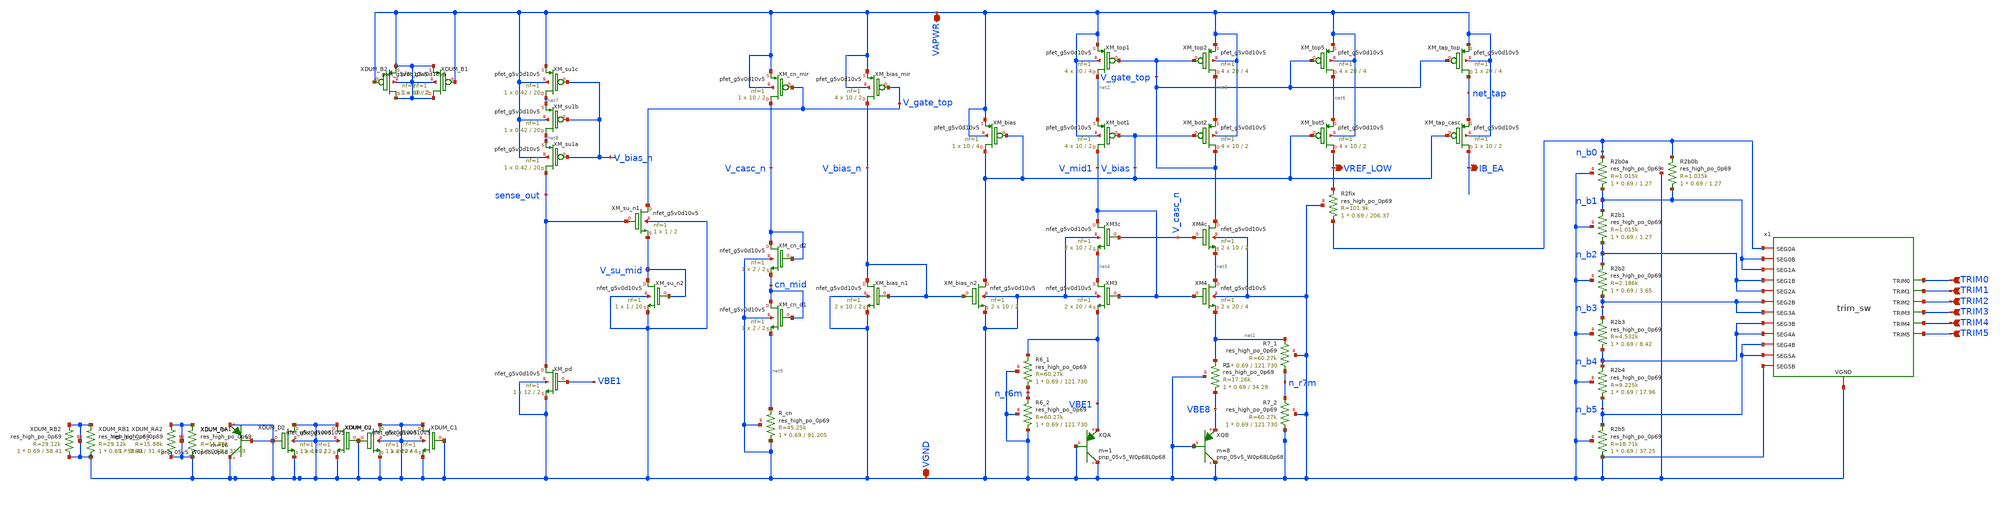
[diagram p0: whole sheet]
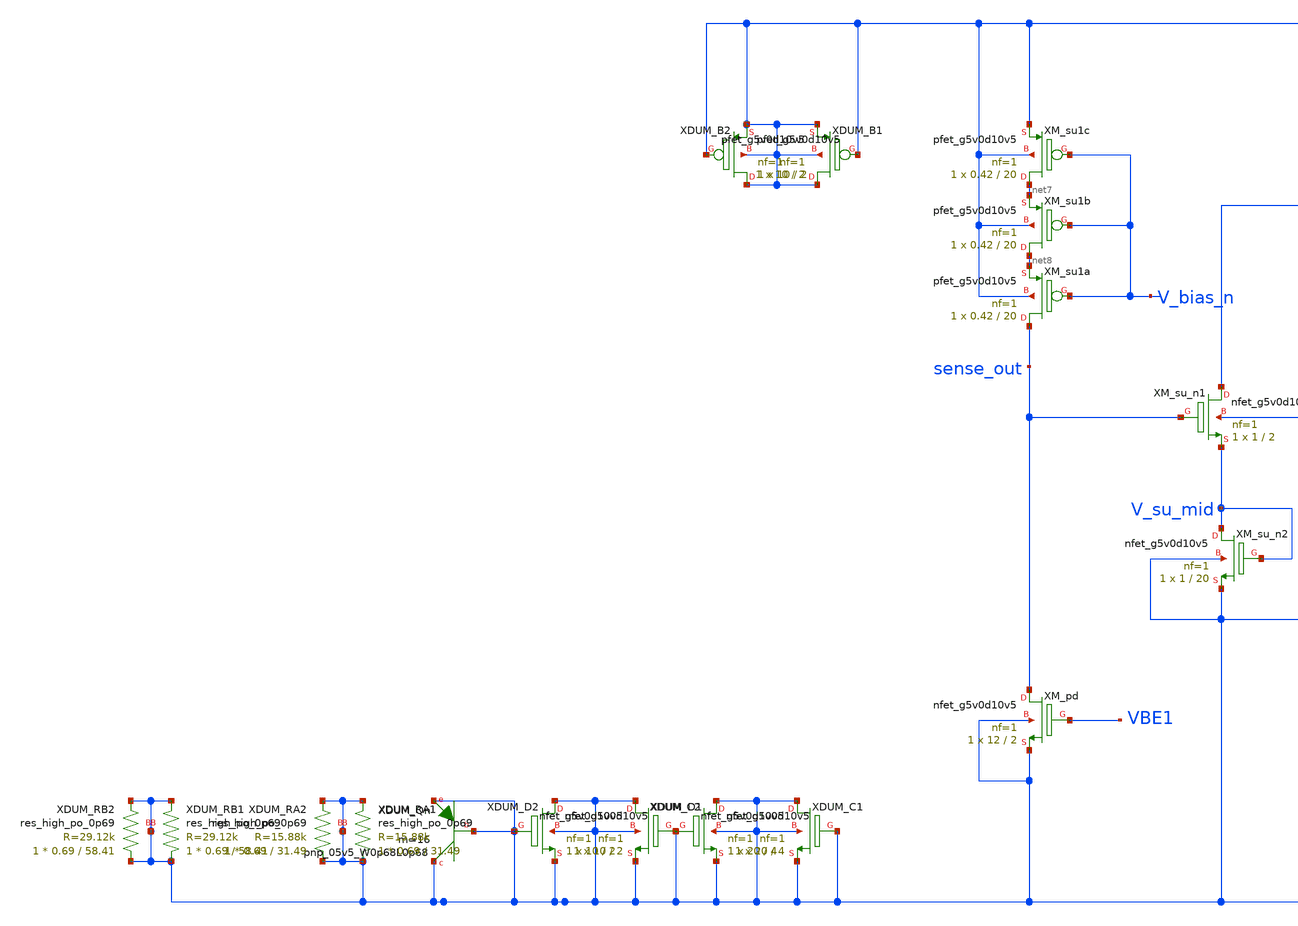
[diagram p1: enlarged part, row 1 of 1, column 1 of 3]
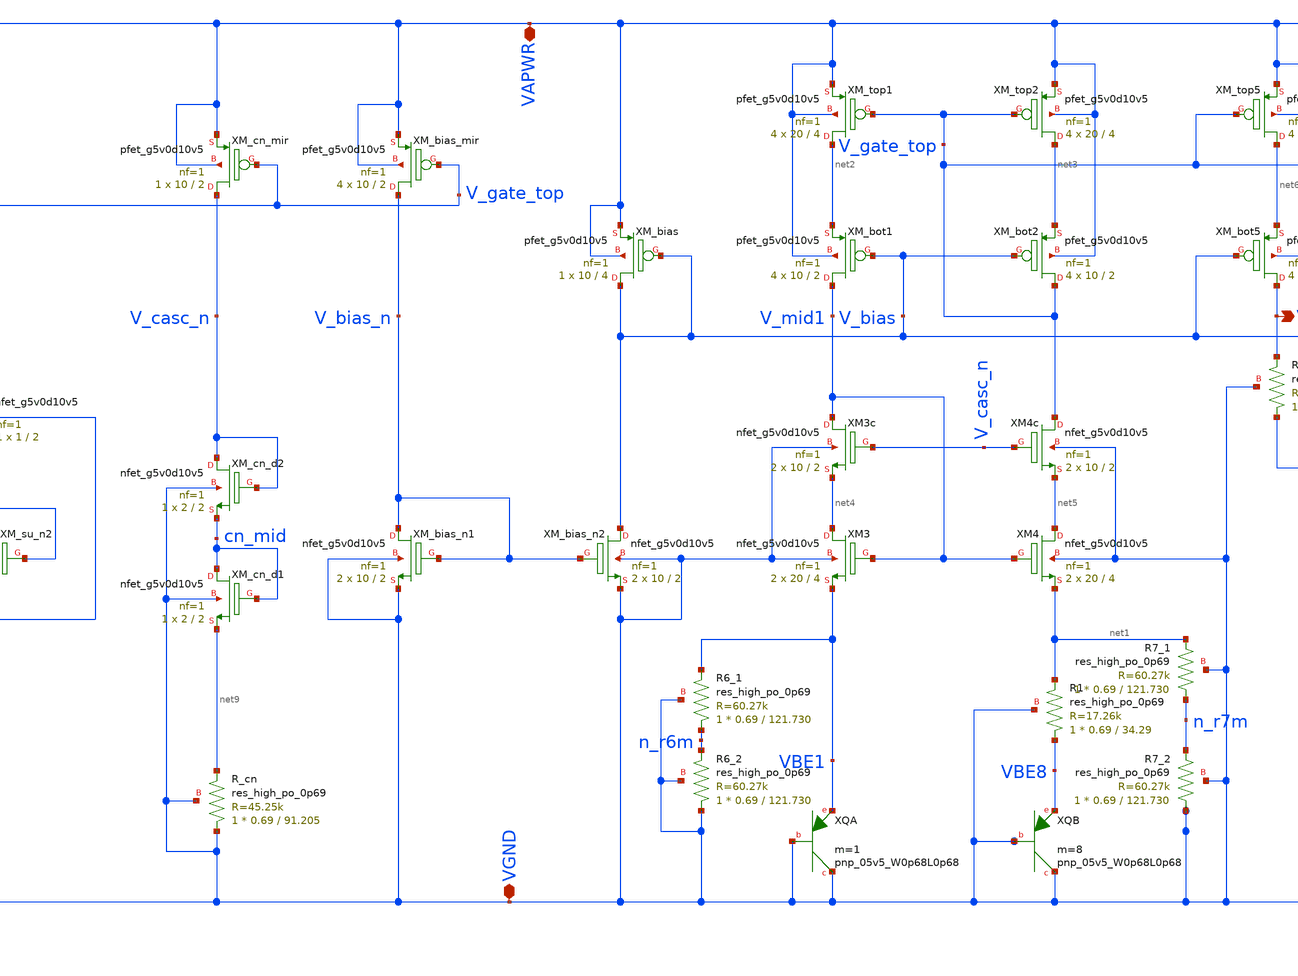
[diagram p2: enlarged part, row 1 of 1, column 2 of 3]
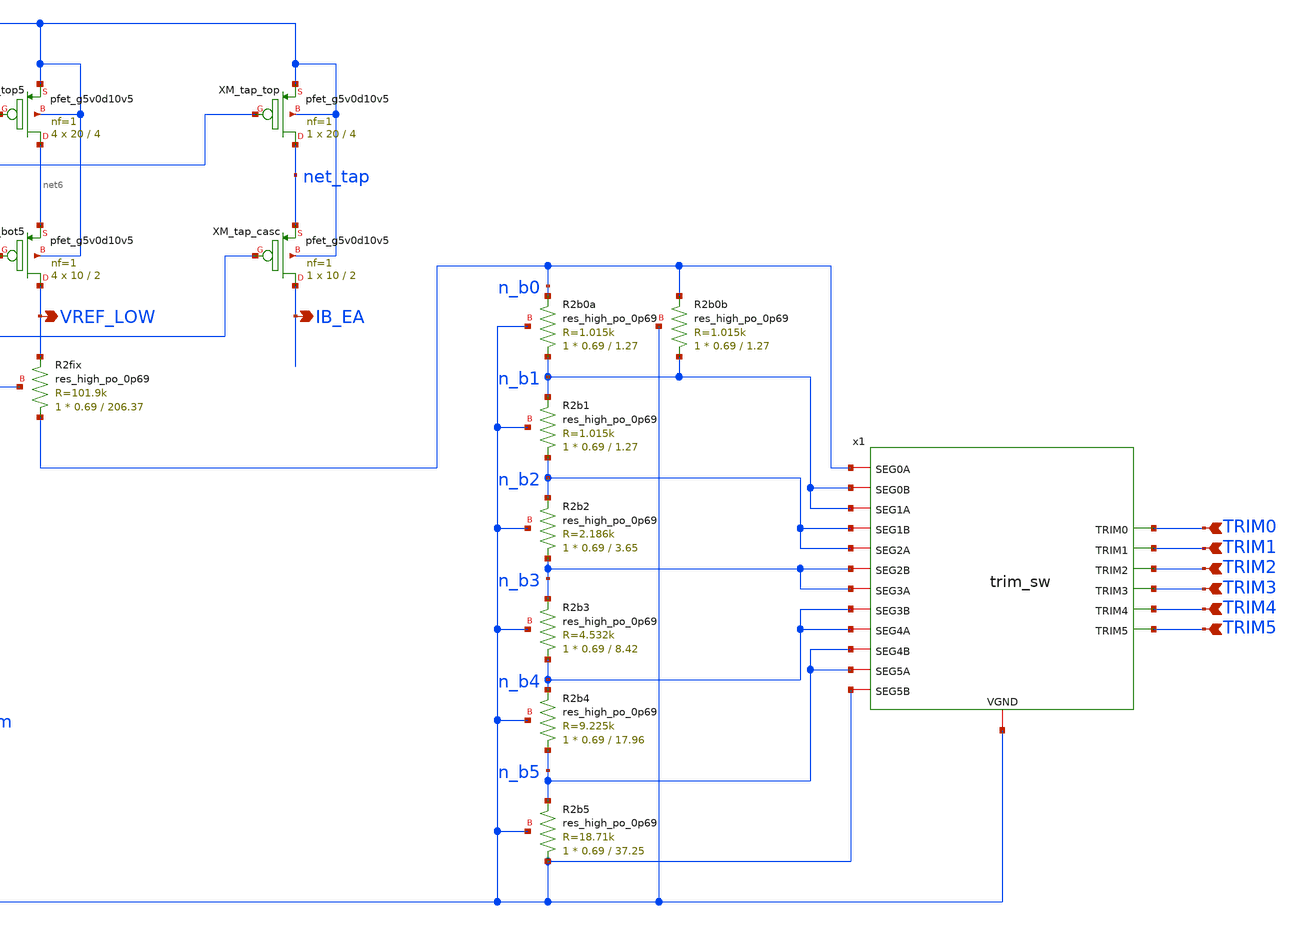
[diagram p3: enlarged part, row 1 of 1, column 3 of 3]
** sch_path: designs/bgr_ldo/bgr/bgr_core.sch
**.subckt bgr_core VAPWR VREF_LOW VGND IB_EA TRIM0 TRIM1 TRIM2 TRIM3 TRIM4 TRIM5
*.iopin VAPWR
*.opin VREF_LOW
*.iopin VGND
*.opin IB_EA
*.ipin TRIM0
*.ipin TRIM1
*.ipin TRIM2
*.ipin TRIM3
*.ipin TRIM4
*.ipin TRIM5
XXQA VGND VGND VBE1 sky130_fd_pr__pnp_05v5_W0p68L0p68 m=1
XXQB VGND VGND VBE8 sky130_fd_pr__pnp_05v5_W0p68L0p68 m=8
XXM_top1 net2 V_gate_top VAPWR VAPWR sky130_fd_pr__pfet_g5v0d10v5 L=4 W=20 nf=1 ad='int((1 + 1)/2) * 20 / 1 * 0.29'
+ as='int((1 + 2)/2) * 20 / 1 * 0.29' pd='2*int((1 + 1)/2) * (20 / 1 + 0.29)' ps='2*int((1 + 2)/2) * (20 / 1 + 0.29)'
+ nrd='0.29 / 20 ' nrs='0.29 / 20 ' sa=0 sb=0 sd=0 mult=4 m=4
XXM_top2 net3 V_gate_top VAPWR VAPWR sky130_fd_pr__pfet_g5v0d10v5 L=4 W=20 nf=1 ad='int((1 + 1)/2) * 20 / 1 * 0.29'
+ as='int((1 + 2)/2) * 20 / 1 * 0.29' pd='2*int((1 + 1)/2) * (20 / 1 + 0.29)' ps='2*int((1 + 2)/2) * (20 / 1 + 0.29)'
+ nrd='0.29 / 20 ' nrs='0.29 / 20 ' sa=0 sb=0 sd=0 mult=4 m=4
XXM_top5 net6 V_gate_top VAPWR VAPWR sky130_fd_pr__pfet_g5v0d10v5 L=4 W=20 nf=1 ad='int((1 + 1)/2) * 20 / 1 * 0.29'
+ as='int((1 + 2)/2) * 20 / 1 * 0.29' pd='2*int((1 + 1)/2) * (20 / 1 + 0.29)' ps='2*int((1 + 2)/2) * (20 / 1 + 0.29)'
+ nrd='0.29 / 20 ' nrs='0.29 / 20 ' sa=0 sb=0 sd=0 mult=4 m=4
XXM3 net4 V_mid1 VBE1 VGND sky130_fd_pr__nfet_g5v0d10v5 L=4 W=20 nf=1 ad='int((1 + 1)/2) * 20 / 1 * 0.29'
+ as='int((1 + 2)/2) * 20 / 1 * 0.29' pd='2*int((1 + 1)/2) * (20 / 1 + 0.29)' ps='2*int((1 + 2)/2) * (20 / 1 + 0.29)'
+ nrd='0.29 / 20 ' nrs='0.29 / 20 ' sa=0 sb=0 sd=0 mult=2 m=2
XXM4 net5 V_mid1 net1 VGND sky130_fd_pr__nfet_g5v0d10v5 L=4 W=20 nf=1 ad='int((1 + 1)/2) * 20 / 1 * 0.29'
+ as='int((1 + 2)/2) * 20 / 1 * 0.29' pd='2*int((1 + 1)/2) * (20 / 1 + 0.29)' ps='2*int((1 + 2)/2) * (20 / 1 + 0.29)'
+ nrd='0.29 / 20 ' nrs='0.29 / 20 ' sa=0 sb=0 sd=0 mult=2 m=2
XXM_bot1 V_mid1 V_bias net2 VAPWR sky130_fd_pr__pfet_g5v0d10v5 L=2 W=10 nf=1 ad='int((1 + 1)/2) * 10 / 1 * 0.29'
+ as='int((1 + 2)/2) * 10 / 1 * 0.29' pd='2*int((1 + 1)/2) * (10 / 1 + 0.29)' ps='2*int((1 + 2)/2) * (10 / 1 + 0.29)'
+ nrd='0.29 / 10 ' nrs='0.29 / 10 ' sa=0 sb=0 sd=0 mult=4 m=4
XXM_bot2 V_gate_top V_bias net3 VAPWR sky130_fd_pr__pfet_g5v0d10v5 L=2 W=10 nf=1 ad='int((1 + 1)/2) * 10 / 1 * 0.29'
+ as='int((1 + 2)/2) * 10 / 1 * 0.29' pd='2*int((1 + 1)/2) * (10 / 1 + 0.29)' ps='2*int((1 + 2)/2) * (10 / 1 + 0.29)'
+ nrd='0.29 / 10 ' nrs='0.29 / 10 ' sa=0 sb=0 sd=0 mult=4 m=4
XXM_bot5 VREF_LOW V_bias net6 VAPWR sky130_fd_pr__pfet_g5v0d10v5 L=2 W=10 nf=1 ad='int((1 + 1)/2) * 10 / 1 * 0.29'
+ as='int((1 + 2)/2) * 10 / 1 * 0.29' pd='2*int((1 + 1)/2) * (10 / 1 + 0.29)' ps='2*int((1 + 2)/2) * (10 / 1 + 0.29)'
+ nrd='0.29 / 10 ' nrs='0.29 / 10 ' sa=0 sb=0 sd=0 mult=4 m=4
XXM_bias V_bias V_bias VAPWR VAPWR sky130_fd_pr__pfet_g5v0d10v5 L=4 W=10 nf=1 ad='int((1 + 1)/2) * 10 / 1 * 0.29'
+ as='int((1 + 2)/2) * 10 / 1 * 0.29' pd='2*int((1 + 1)/2) * (10 / 1 + 0.29)' ps='2*int((1 + 2)/2) * (10 / 1 + 0.29)'
+ nrd='0.29 / 10 ' nrs='0.29 / 10 ' sa=0 sb=0 sd=0 mult=1 m=1
XXM_bias_mir V_bias_n V_gate_top VAPWR VAPWR sky130_fd_pr__pfet_g5v0d10v5 L=2 W=10 nf=1 ad='int((1 + 1)/2) * 10 / 1 * 0.29'
+ as='int((1 + 2)/2) * 10 / 1 * 0.29' pd='2*int((1 + 1)/2) * (10 / 1 + 0.29)' ps='2*int((1 + 2)/2) * (10 / 1 + 0.29)'
+ nrd='0.29 / 10 ' nrs='0.29 / 10 ' sa=0 sb=0 sd=0 mult=4 m=4
XXM_bias_n1 V_bias_n V_bias_n VGND VGND sky130_fd_pr__nfet_g5v0d10v5 L=2 W=10 nf=1 ad='int((1 + 1)/2) * 10 / 1 * 0.29'
+ as='int((1 + 2)/2) * 10 / 1 * 0.29' pd='2*int((1 + 1)/2) * (10 / 1 + 0.29)' ps='2*int((1 + 2)/2) * (10 / 1 + 0.29)'
+ nrd='0.29 / 10 ' nrs='0.29 / 10 ' sa=0 sb=0 sd=0 mult=2 m=2
XXM_bias_n2 V_bias V_bias_n VGND VGND sky130_fd_pr__nfet_g5v0d10v5 L=2 W=10 nf=1 ad='int((1 + 1)/2) * 10 / 1 * 0.29'
+ as='int((1 + 2)/2) * 10 / 1 * 0.29' pd='2*int((1 + 1)/2) * (10 / 1 + 0.29)' ps='2*int((1 + 2)/2) * (10 / 1 + 0.29)'
+ nrd='0.29 / 10 ' nrs='0.29 / 10 ' sa=0 sb=0 sd=0 mult=2 m=2
XXM_su_n1 V_gate_top sense_out V_su_mid VGND sky130_fd_pr__nfet_g5v0d10v5 L=2 W=1 nf=1 ad='int((1 + 1)/2) * 1 / 1 * 0.29'
+ as='int((1 + 2)/2) * 1 / 1 * 0.29' pd='2*int((1 + 1)/2) * (1 / 1 + 0.29)' ps='2*int((1 + 2)/2) * (1 / 1 + 0.29)'
+ nrd='0.29 / 1 ' nrs='0.29 / 1 ' sa=0 sb=0 sd=0 mult=1 m=1
XXM_su_n2 V_su_mid V_su_mid VGND VGND sky130_fd_pr__nfet_g5v0d10v5 L=20 W=1 nf=1 ad='int((1 + 1)/2) * 1 / 1 * 0.29'
+ as='int((1 + 2)/2) * 1 / 1 * 0.29' pd='2*int((1 + 1)/2) * (1 / 1 + 0.29)' ps='2*int((1 + 2)/2) * (1 / 1 + 0.29)'
+ nrd='0.29 / 1 ' nrs='0.29 / 1 ' sa=0 sb=0 sd=0 mult=1 m=1
XXM_pd sense_out VBE1 VGND VGND sky130_fd_pr__nfet_g5v0d10v5 L=2 W=12 nf=1 ad='int((1 + 1)/2) * 12 / 1 * 0.29'
+ as='int((1 + 2)/2) * 12 / 1 * 0.29' pd='2*int((1 + 1)/2) * (12 / 1 + 0.29)' ps='2*int((1 + 2)/2) * (12 / 1 + 0.29)'
+ nrd='0.29 / 12 ' nrs='0.29 / 12 ' sa=0 sb=0 sd=0 mult=1 m=1
XXM_su1a sense_out V_bias_n net8 VAPWR sky130_fd_pr__pfet_g5v0d10v5 L=20 W=0.42 nf=1 ad='int((1 + 1)/2) * 0.42 / 1 * 0.29'
+ as='int((1 + 2)/2) * 0.42 / 1 * 0.29' pd='2*int((1 + 1)/2) * (0.42 / 1 + 0.29)' ps='2*int((1 + 2)/2) * (0.42 / 1 + 0.29)'
+ nrd='0.29 / 0.42 ' nrs='0.29 / 0.42 ' sa=0 sb=0 sd=0 mult=1 m=1
XXM_su1b net8 V_bias_n net7 VAPWR sky130_fd_pr__pfet_g5v0d10v5 L=20 W=0.42 nf=1 ad='int((1 + 1)/2) * 0.42 / 1 * 0.29'
+ as='int((1 + 2)/2) * 0.42 / 1 * 0.29' pd='2*int((1 + 1)/2) * (0.42 / 1 + 0.29)' ps='2*int((1 + 2)/2) * (0.42 / 1 + 0.29)'
+ nrd='0.29 / 0.42 ' nrs='0.29 / 0.42 ' sa=0 sb=0 sd=0 mult=1 m=1
XXM_su1c net7 V_bias_n VAPWR VAPWR sky130_fd_pr__pfet_g5v0d10v5 L=20 W=0.42 nf=1 ad='int((1 + 1)/2) * 0.42 / 1 * 0.29'
+ as='int((1 + 2)/2) * 0.42 / 1 * 0.29' pd='2*int((1 + 1)/2) * (0.42 / 1 + 0.29)' ps='2*int((1 + 2)/2) * (0.42 / 1 + 0.29)'
+ nrd='0.29 / 0.42 ' nrs='0.29 / 0.42 ' sa=0 sb=0 sd=0 mult=1 m=1
XR1 VBE8 net1 VGND sky130_fd_pr__res_high_po_0p69 L=34.29 mult=1 m=1
XR6_1 n_r6m VBE1 VGND sky130_fd_pr__res_high_po_0p69 L=121.730 mult=1 m=1
XR7_1 n_r7m net1 VGND sky130_fd_pr__res_high_po_0p69 L=121.730 mult=1 m=1
XR2fix n_b0 VREF_LOW VGND sky130_fd_pr__res_high_po_0p69 L=206.37 mult=1 m=1
XXM3c V_mid1 V_casc_n net4 VGND sky130_fd_pr__nfet_g5v0d10v5 L=2 W=10 nf=1 ad='int((1 + 1)/2) * 10 / 1 * 0.29'
+ as='int((1 + 2)/2) * 10 / 1 * 0.29' pd='2*int((1 + 1)/2) * (10 / 1 + 0.29)' ps='2*int((1 + 2)/2) * (10 / 1 + 0.29)'
+ nrd='0.29 / 10 ' nrs='0.29 / 10 ' sa=0 sb=0 sd=0 mult=2 m=2
XXM4c V_gate_top V_casc_n net5 VGND sky130_fd_pr__nfet_g5v0d10v5 L=2 W=10 nf=1 ad='int((1 + 1)/2) * 10 / 1 * 0.29'
+ as='int((1 + 2)/2) * 10 / 1 * 0.29' pd='2*int((1 + 1)/2) * (10 / 1 + 0.29)' ps='2*int((1 + 2)/2) * (10 / 1 + 0.29)'
+ nrd='0.29 / 10 ' nrs='0.29 / 10 ' sa=0 sb=0 sd=0 mult=2 m=2
XXM_cn_mir V_casc_n V_gate_top VAPWR VAPWR sky130_fd_pr__pfet_g5v0d10v5 L=2 W=10 nf=1 ad='int((1 + 1)/2) * 10 / 1 * 0.29'
+ as='int((1 + 2)/2) * 10 / 1 * 0.29' pd='2*int((1 + 1)/2) * (10 / 1 + 0.29)' ps='2*int((1 + 2)/2) * (10 / 1 + 0.29)'
+ nrd='0.29 / 10 ' nrs='0.29 / 10 ' sa=0 sb=0 sd=0 mult=1 m=1
XXM_cn_d2 V_casc_n V_casc_n cn_mid VGND sky130_fd_pr__nfet_g5v0d10v5 L=2 W=2 nf=1 ad='int((1 + 1)/2) * 2 / 1 * 0.29'
+ as='int((1 + 2)/2) * 2 / 1 * 0.29' pd='2*int((1 + 1)/2) * (2 / 1 + 0.29)' ps='2*int((1 + 2)/2) * (2 / 1 + 0.29)'
+ nrd='0.29 / 2 ' nrs='0.29 / 2 ' sa=0 sb=0 sd=0 mult=1 m=1
XXM_cn_d1 cn_mid cn_mid net9 VGND sky130_fd_pr__nfet_g5v0d10v5 L=2 W=2 nf=1 ad='int((1 + 1)/2) * 2 / 1 * 0.29'
+ as='int((1 + 2)/2) * 2 / 1 * 0.29' pd='2*int((1 + 1)/2) * (2 / 1 + 0.29)' ps='2*int((1 + 2)/2) * (2 / 1 + 0.29)'
+ nrd='0.29 / 2 ' nrs='0.29 / 2 ' sa=0 sb=0 sd=0 mult=1 m=1
XR_cn VGND net9 VGND sky130_fd_pr__res_high_po_0p69 L=91.205 mult=1 m=1
XXM_tap_top net_tap V_gate_top VAPWR VAPWR sky130_fd_pr__pfet_g5v0d10v5 L=4 W=20 nf=1 ad='int((1 + 1)/2) * 20 / 1 * 0.29'
+ as='int((1 + 2)/2) * 20 / 1 * 0.29' pd='2*int((1 + 1)/2) * (20 / 1 + 0.29)' ps='2*int((1 + 2)/2) * (20 / 1 + 0.29)'
+ nrd='0.29 / 20 ' nrs='0.29 / 20 ' sa=0 sb=0 sd=0 mult=1 m=1
XXM_tap_casc IB_EA V_bias net_tap VAPWR sky130_fd_pr__pfet_g5v0d10v5 L=2 W=10 nf=1 ad='int((1 + 1)/2) * 10 / 1 * 0.29'
+ as='int((1 + 2)/2) * 10 / 1 * 0.29' pd='2*int((1 + 1)/2) * (10 / 1 + 0.29)' ps='2*int((1 + 2)/2) * (10 / 1 + 0.29)'
+ nrd='0.29 / 10 ' nrs='0.29 / 10 ' sa=0 sb=0 sd=0 mult=1 m=1
XR2b0a n_b1 n_b0 VGND sky130_fd_pr__res_high_po_0p69 L=1.27 mult=1 m=1
XR2b1 n_b2 n_b1 VGND sky130_fd_pr__res_high_po_0p69 L=1.27 mult=1 m=1
XR2b2 n_b3 n_b2 VGND sky130_fd_pr__res_high_po_0p69 L=3.65 mult=1 m=1
XR2b5 VGND n_b5 VGND sky130_fd_pr__res_high_po_0p69 L=37.25 mult=1 m=1
x1 VGND n_b4 n_b2 n_b0 n_b5 n_b1 n_b3 TRIM1 TRIM3 TRIM0 TRIM2 TRIM5 TRIM4 n_b5 n_b4 VGND n_b2 n_b3
+ n_b1 trim_sw
XR6_2 VGND n_r6m VGND sky130_fd_pr__res_high_po_0p69 L=121.730 mult=1 m=1
XR7_2 VGND n_r7m VGND sky130_fd_pr__res_high_po_0p69 L=121.730 mult=1 m=1
XXDUM_B1 VAPWR VAPWR VAPWR VAPWR sky130_fd_pr__pfet_g5v0d10v5 L=2 W=10 nf=1 ad='int((1 + 1)/2) * 10 / 1 * 0.29'
+ as='int((1 + 2)/2) * 10 / 1 * 0.29' pd='2*int((1 + 1)/2) * (10 / 1 + 0.29)' ps='2*int((1 + 2)/2) * (10 / 1 + 0.29)'
+ nrd='0.29 / 10 ' nrs='0.29 / 10 ' sa=0 sb=0 sd=0 mult=1 m=1
XXDUM_B2 VAPWR VAPWR VAPWR VAPWR sky130_fd_pr__pfet_g5v0d10v5 L=2 W=10 nf=1 ad='int((1 + 1)/2) * 10 / 1 * 0.29'
+ as='int((1 + 2)/2) * 10 / 1 * 0.29' pd='2*int((1 + 1)/2) * (10 / 1 + 0.29)' ps='2*int((1 + 2)/2) * (10 / 1 + 0.29)'
+ nrd='0.29 / 10 ' nrs='0.29 / 10 ' sa=0 sb=0 sd=0 mult=1 m=1
XXDUM_C1 VGND VGND VGND VGND sky130_fd_pr__nfet_g5v0d10v5 L=4 W=20 nf=1 ad='int((1 + 1)/2) * 20 / 1 * 0.29'
+ as='int((1 + 2)/2) * 20 / 1 * 0.29' pd='2*int((1 + 1)/2) * (20 / 1 + 0.29)' ps='2*int((1 + 2)/2) * (20 / 1 + 0.29)'
+ nrd='0.29 / 20 ' nrs='0.29 / 20 ' sa=0 sb=0 sd=0 mult=1 m=1
XXDUM_C2 VGND VGND VGND VGND sky130_fd_pr__nfet_g5v0d10v5 L=4 W=20 nf=1 ad='int((1 + 1)/2) * 20 / 1 * 0.29'
+ as='int((1 + 2)/2) * 20 / 1 * 0.29' pd='2*int((1 + 1)/2) * (20 / 1 + 0.29)' ps='2*int((1 + 2)/2) * (20 / 1 + 0.29)'
+ nrd='0.29 / 20 ' nrs='0.29 / 20 ' sa=0 sb=0 sd=0 mult=1 m=1
XXDUM_D1 VGND VGND VGND VGND sky130_fd_pr__nfet_g5v0d10v5 L=2 W=10 nf=1 ad='int((1 + 1)/2) * 10 / 1 * 0.29'
+ as='int((1 + 2)/2) * 10 / 1 * 0.29' pd='2*int((1 + 1)/2) * (10 / 1 + 0.29)' ps='2*int((1 + 2)/2) * (10 / 1 + 0.29)'
+ nrd='0.29 / 10 ' nrs='0.29 / 10 ' sa=0 sb=0 sd=0 mult=1 m=1
XXDUM_D2 VGND VGND VGND VGND sky130_fd_pr__nfet_g5v0d10v5 L=2 W=10 nf=1 ad='int((1 + 1)/2) * 10 / 1 * 0.29'
+ as='int((1 + 2)/2) * 10 / 1 * 0.29' pd='2*int((1 + 1)/2) * (10 / 1 + 0.29)' ps='2*int((1 + 2)/2) * (10 / 1 + 0.29)'
+ nrd='0.29 / 10 ' nrs='0.29 / 10 ' sa=0 sb=0 sd=0 mult=1 m=1
XXDUM_Qn VGND VGND VGND sky130_fd_pr__pnp_05v5_W0p68L0p68 m=16
XXDUM_RA1 VGND VGND VGND sky130_fd_pr__res_high_po_0p69 L=31.49 mult=1 m=1
XXDUM_RA2 VGND VGND VGND sky130_fd_pr__res_high_po_0p69 L=31.49 mult=1 m=1
XXDUM_RB1 VGND VGND VGND sky130_fd_pr__res_high_po_0p69 L=58.41 mult=1 m=1
XXDUM_RB2 VGND VGND VGND sky130_fd_pr__res_high_po_0p69 L=58.41 mult=1 m=1
XR2b3 n_b4 n_b3 VGND sky130_fd_pr__res_high_po_0p69 L=8.42 mult=1 m=1
XR2b4 n_b5 n_b4 VGND sky130_fd_pr__res_high_po_0p69 L=17.96 mult=1 m=1
XR2b0b n_b1 n_b0 VGND sky130_fd_pr__res_high_po_0p69 L=1.27 mult=1 m=1
**.ends

* expanding   symbol:  trim_sw.sym # of pins=19
** sym_path: designs/bgr_ldo/bgr/trim_sw.sym
** sch_path: designs/bgr_ldo/bgr/trim_sw.sch
.subckt trim_sw VGND SEG4A SEG2A SEG0A SEG5A SEG1A SEG3A TRIM1 TRIM3 TRIM0 TRIM2 TRIM5 TRIM4 SEG4B
+ SEG3B SEG5B SEG1B SEG2B SEG0B
*.ipin TRIM0
*.ipin TRIM2
*.ipin TRIM3
*.ipin TRIM4
*.iopin SEG0A
*.iopin SEG0B
*.iopin SEG2A
*.iopin SEG3A
*.iopin SEG4A
*.iopin SEG2B
*.iopin SEG3B
*.iopin SEG4B
*.iopin VGND
*.ipin TRIM1
*.iopin SEG1A
*.iopin SEG1B
*.ipin TRIM5
*.iopin SEG5A
*.iopin SEG5B
XSWb0 SEG0A TRIM0 SEG0B VGND sky130_fd_pr__nfet_01v8 L=0.15 W=10 nf=1 ad='int((1 + 1)/2) * 10 / 1 * 0.29'
+ as='int((1 + 2)/2) * 10 / 1 * 0.29' pd='2*int((1 + 1)/2) * (10 / 1 + 0.29)' ps='2*int((1 + 2)/2) * (10 / 1 + 0.29)'
+ nrd='0.29 / 10 ' nrs='0.29 / 10 ' sa=0 sb=0 sd=0 mult=22 m=22
XSWb2 SEG2A TRIM2 SEG2B VGND sky130_fd_pr__nfet_01v8 L=0.15 W=10 nf=1 ad='int((1 + 1)/2) * 10 / 1 * 0.29'
+ as='int((1 + 2)/2) * 10 / 1 * 0.29' pd='2*int((1 + 1)/2) * (10 / 1 + 0.29)' ps='2*int((1 + 2)/2) * (10 / 1 + 0.29)'
+ nrd='0.29 / 10 ' nrs='0.29 / 10 ' sa=0 sb=0 sd=0 mult=22 m=22
XSWb3 SEG3A TRIM3 SEG3B VGND sky130_fd_pr__nfet_01v8 L=0.15 W=10 nf=1 ad='int((1 + 1)/2) * 10 / 1 * 0.29'
+ as='int((1 + 2)/2) * 10 / 1 * 0.29' pd='2*int((1 + 1)/2) * (10 / 1 + 0.29)' ps='2*int((1 + 2)/2) * (10 / 1 + 0.29)'
+ nrd='0.29 / 10 ' nrs='0.29 / 10 ' sa=0 sb=0 sd=0 mult=22 m=22
XSWb4 SEG4A TRIM4 SEG4B VGND sky130_fd_pr__nfet_01v8 L=0.15 W=10 nf=1 ad='int((1 + 1)/2) * 10 / 1 * 0.29'
+ as='int((1 + 2)/2) * 10 / 1 * 0.29' pd='2*int((1 + 1)/2) * (10 / 1 + 0.29)' ps='2*int((1 + 2)/2) * (10 / 1 + 0.29)'
+ nrd='0.29 / 10 ' nrs='0.29 / 10 ' sa=0 sb=0 sd=0 mult=22 m=22
XSWb1 SEG1A TRIM1 SEG1B VGND sky130_fd_pr__nfet_01v8 L=0.15 W=10 nf=1 ad='int((1 + 1)/2) * 10 / 1 * 0.29'
+ as='int((1 + 2)/2) * 10 / 1 * 0.29' pd='2*int((1 + 1)/2) * (10 / 1 + 0.29)' ps='2*int((1 + 2)/2) * (10 / 1 + 0.29)'
+ nrd='0.29 / 10 ' nrs='0.29 / 10 ' sa=0 sb=0 sd=0 mult=22 m=22
XSWb5 SEG5A TRIM5 SEG5B VGND sky130_fd_pr__nfet_01v8 L=0.15 W=10 nf=1 ad='int((1 + 1)/2) * 10 / 1 * 0.29'
+ as='int((1 + 2)/2) * 10 / 1 * 0.29' pd='2*int((1 + 1)/2) * (10 / 1 + 0.29)' ps='2*int((1 + 2)/2) * (10 / 1 + 0.29)'
+ nrd='0.29 / 10 ' nrs='0.29 / 10 ' sa=0 sb=0 sd=0 mult=6 m=6
.ends

.end
